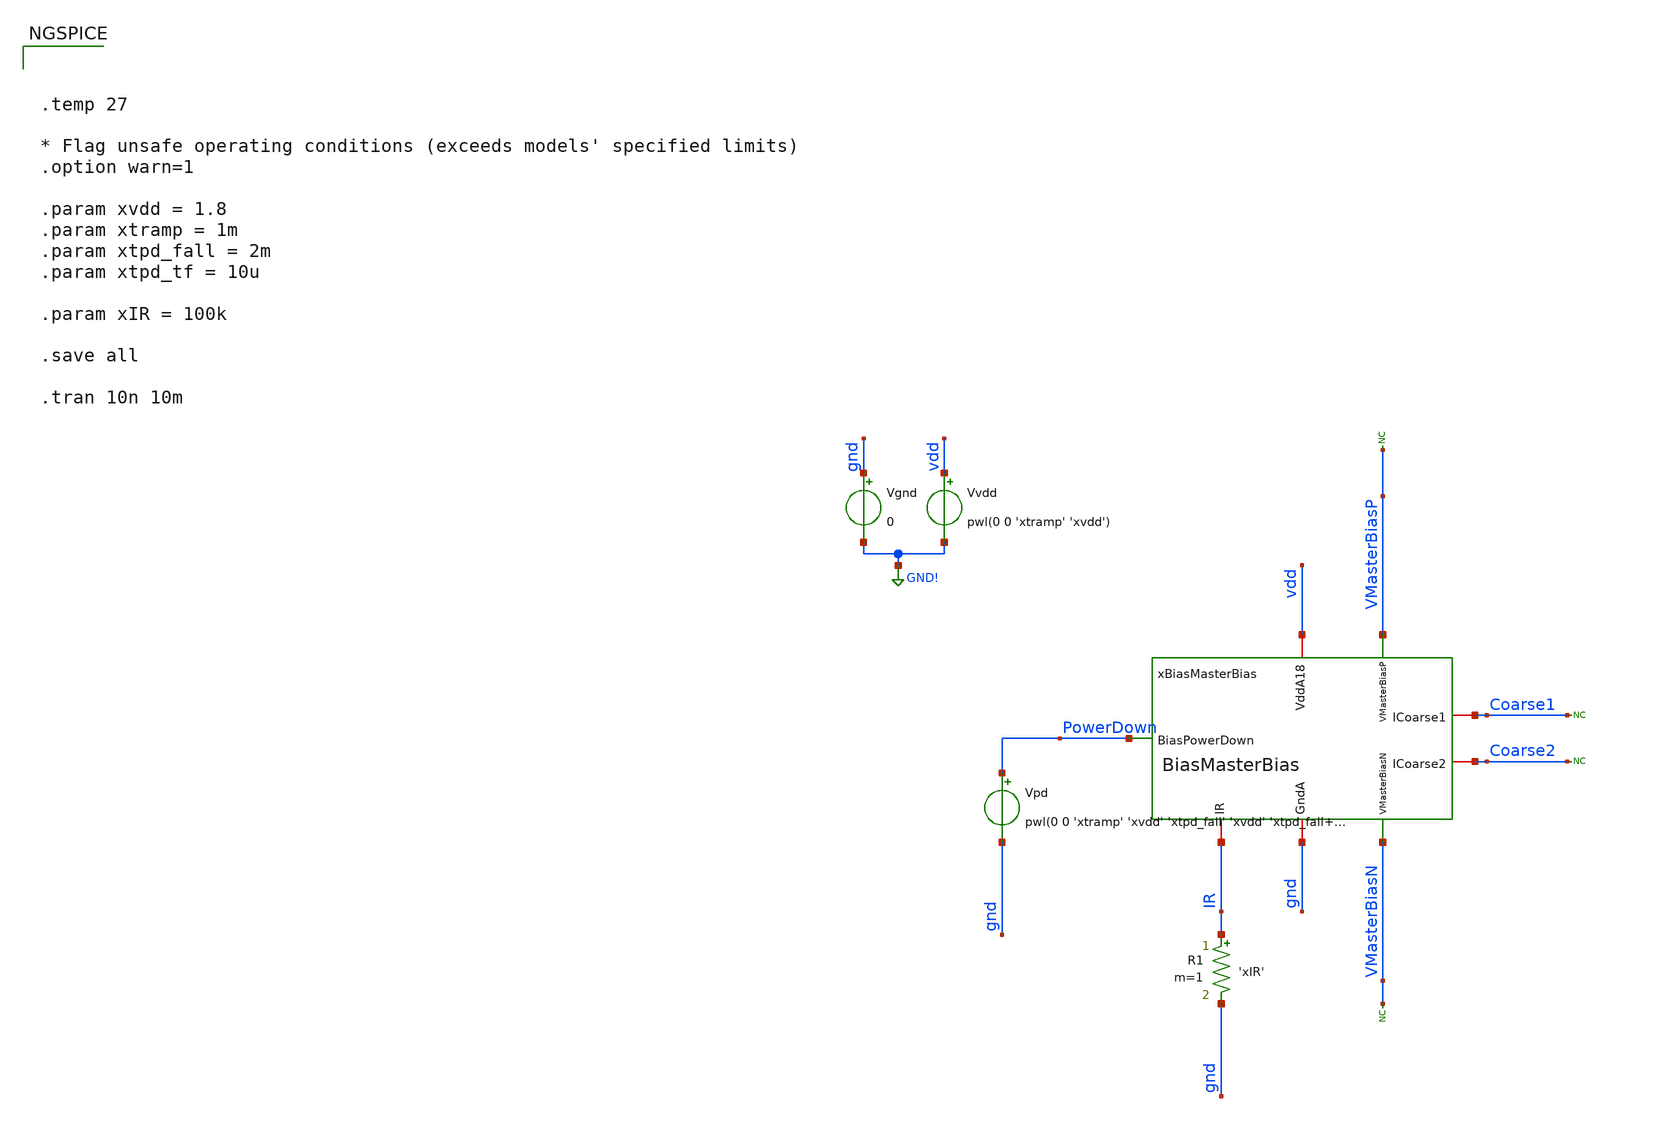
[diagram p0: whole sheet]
** sch_path: analog/klayout/production/final_merge_20260923/testbenches/cace/analog/xschem/tb_BiasMasterBias_bootstrap.sch
**.subckt tb_BiasMasterBias_bootstrap
xBiasMasterBias VMasterBiasP Coarse2 Coarse1 VMasterBiasN PowerDown vdd gnd IR BiasMasterBias
Vgnd gnd GND! 0
.save i(vgnd)
Vvdd vdd GND! pwl(0 0 'xtramp' 'xvdd')
.save i(vvdd)
* noconn VMasterBiasP
* noconn Coarse1
* noconn Coarse2
* noconn VMasterBiasN
R1 IR gnd 'xIR' m=1
Vpd PowerDown gnd pwl(0 0 'xtramp' 'xvdd' 'xtpd_fall' 'xvdd' 'xtpd_fall+xtpd_tf' 0)
.save i(vpd)
**** begin user architecture code

** opencircuitdesign pdks install
.lib $::SKYWATER_MODELS/sky130.lib.spice tt




.temp 27

* Flag unsafe operating conditions (exceeds models' specified limits)
.option warn=1

.param xvdd = 1.8
.param xtramp = 1m
.param xtpd_fall = 2m
.param xtpd_tf = 10u

.param xIR = 100k

.save all

.tran 10n 10m


**** end user architecture code
**.ends

* expanding   symbol:  BiasMasterBias.sym # of pins=8
** sym_path: analog/xschem/BiasMasterBias.sym
** sch_path: analog/xschem/BiasMasterBias.sch
.subckt BiasMasterBias VMasterBiasP ICoarse2 ICoarse1 VMasterBiasN BiasPowerDown VddA18 GndA IR
*.opin VMasterBiasP
*.iopin IR
*.iopin VddA18
*.iopin GndA
*.opin VMasterBiasN
*.iopin ICoarse1
*.iopin ICoarse2
*.ipin BiasPowerDown
XMNBiasDio VMasterBiasN VMasterBiasN GndA GndA sky130_fd_pr__nfet_01v8_lvt L=5 W=20 nf=1 ad='int((1 +
+ 1)/2) * 20 / 1 * 0.29' as='int((1 + 2)/2) * 20 / 1 * 0.29' pd='2*int((1 + 1)/2) * (20 / 1 + 0.29)' ps='2*int((1
+ + 2)/2) * (20 / 1 + 0.29)' nrd='0.29 / 20 ' nrs='0.29 / 20 ' sa=0 sb=0 sd=0 mult=12 m=12
XMPBias VCasc VMasterBiasP VddA18 VddA18 sky130_fd_pr__pfet_01v8 L=20 W=2 nf=1 ad='int((1 + 1)/2) * 2
+ / 1 * 0.29' as='int((1 + 2)/2) * 2 / 1 * 0.29' pd='2*int((1 + 1)/2) * (2 / 1 + 0.29)' ps='2*int((1 +
+ 2)/2) * (2 / 1 + 0.29)' nrd='0.29 / 2 ' nrs='0.29 / 2 ' sa=0 sb=0 sd=0 mult=8 m=8
XMNBias net1 VMasterBiasN IR GndA sky130_fd_pr__nfet_01v8_lvt L=5 W=20 nf=1 ad='int((1 + 1)/2) * 20 /
+ 1 * 0.29' as='int((1 + 2)/2) * 20 / 1 * 0.29' pd='2*int((1 + 1)/2) * (20 / 1 + 0.29)' ps='2*int((1 +
+ 2)/2) * (20 / 1 + 0.29)' nrd='0.29 / 20 ' nrs='0.29 / 20 ' sa=0 sb=0 sd=0 mult=16 m=16
XMnBiasCascDio VCasc VCasc VMasterBiasN GndA sky130_fd_pr__nfet_01v8_lvt L=20 W=1 nf=1 ad='int((1 + 1)/2)
+ * 1 / 1 * 0.29' as='int((1 + 2)/2) * 1 / 1 * 0.29' pd='2*int((1 + 1)/2) * (1 / 1 + 0.29)' ps='2*int((1
+ + 2)/2) * (1 / 1 + 0.29)' nrd='0.29 / 1 ' nrs='0.29 / 1 ' sa=0 sb=0 sd=0 mult=12 m=12
XMnBiasCasc VMasterBiasP VCasc net1 GndA sky130_fd_pr__nfet_01v8_lvt L=20 W=1 nf=1 ad='int((1 + 1)/2)
+ * 1 / 1 * 0.29' as='int((1 + 2)/2) * 1 / 1 * 0.29' pd='2*int((1 + 1)/2) * (1 / 1 + 0.29)' ps='2*int((1
+ + 2)/2) * (1 / 1 + 0.29)' nrd='0.29 / 1 ' nrs='0.29 / 1 ' sa=0 sb=0 sd=0 mult=16 m=16
XMPBiasDio VMasterBiasP VMasterBiasP VddA18 VddA18 sky130_fd_pr__pfet_01v8 L=20 W=2 nf=1 ad='int((1 +
+ 1)/2) * 2 / 1 * 0.29' as='int((1 + 2)/2) * 2 / 1 * 0.29' pd='2*int((1 + 1)/2) * (2 / 1 + 0.29)' ps='2*int((1
+ + 2)/2) * (2 / 1 + 0.29)' nrd='0.29 / 2 ' nrs='0.29 / 2 ' sa=0 sb=0 sd=0 mult=8 m=8
XMNMirr1 net2 VMasterBiasN GndA GndA sky130_fd_pr__nfet_01v8_lvt L=5 W=20 nf=1 ad='int((1 + 1)/2) * 20
+ / 1 * 0.29' as='int((1 + 2)/2) * 20 / 1 * 0.29' pd='2*int((1 + 1)/2) * (20 / 1 + 0.29)' ps='2*int((1
+ + 2)/2) * (20 / 1 + 0.29)' nrd='0.29 / 20 ' nrs='0.29 / 20 ' sa=0 sb=0 sd=0 mult=1 m=1
XMNMirrCasc1 ICoarse1 VCasc net2 GndA sky130_fd_pr__nfet_01v8_lvt L=20 W=1 nf=1 ad='int((1 + 1)/2) *
+ 1 / 1 * 0.29' as='int((1 + 2)/2) * 1 / 1 * 0.29' pd='2*int((1 + 1)/2) * (1 / 1 + 0.29)' ps='2*int((1
+ + 2)/2) * (1 / 1 + 0.29)' nrd='0.29 / 1 ' nrs='0.29 / 1 ' sa=0 sb=0 sd=0 mult=1 m=1
XMNMirr2 net3 VMasterBiasN GndA GndA sky130_fd_pr__nfet_01v8_lvt L=5 W=20 nf=1 ad='int((1 + 1)/2) * 20
+ / 1 * 0.29' as='int((1 + 2)/2) * 20 / 1 * 0.29' pd='2*int((1 + 1)/2) * (20 / 1 + 0.29)' ps='2*int((1
+ + 2)/2) * (20 / 1 + 0.29)' nrd='0.29 / 20 ' nrs='0.29 / 20 ' sa=0 sb=0 sd=0 mult=1 m=1
XMNMirrCasc2 ICoarse2 VCasc net3 GndA sky130_fd_pr__nfet_01v8_lvt L=20 W=1 nf=1 ad='int((1 + 1)/2) *
+ 1 / 1 * 0.29' as='int((1 + 2)/2) * 1 / 1 * 0.29' pd='2*int((1 + 1)/2) * (1 / 1 + 0.29)' ps='2*int((1
+ + 2)/2) * (1 / 1 + 0.29)' nrd='0.29 / 1 ' nrs='0.29 / 1 ' sa=0 sb=0 sd=0 mult=1 m=1
XMNBSPD VCasc BiasPowerDown GndA GndA sky130_fd_pr__nfet_01v8_lvt L=0.2 W=2 nf=1 ad='int((1 + 1)/2) *
+ 2 / 1 * 0.29' as='int((1 + 2)/2) * 2 / 1 * 0.29' pd='2*int((1 + 1)/2) * (2 / 1 + 0.29)' ps='2*int((1
+ + 2)/2) * (2 / 1 + 0.29)' nrd='0.29 / 2 ' nrs='0.29 / 2 ' sa=0 sb=0 sd=0 mult=1 m=1
XMNBSCapBias VddA18 VMasterBiasP VddA18 GndA sky130_fd_pr__nfet_01v8 L=16 W=16 nf=1 ad='int((1 + 1)/2)
+ * 16 / 1 * 0.29' as='int((1 + 2)/2) * 16 / 1 * 0.29' pd='2*int((1 + 1)/2) * (16 / 1 + 0.29)' ps='2*int((1
+ + 2)/2) * (16 / 1 + 0.29)' nrd='0.29 / 16 ' nrs='0.29 / 16 ' sa=0 sb=0 sd=0 mult=1 m=1
XMPBS bootstrap VMasterBiasP VddA18 VddA18 sky130_fd_pr__pfet_01v8 L=0.2 W=2 nf=1 ad='int((1 + 1)/2)
+ * 2 / 1 * 0.29' as='int((1 + 2)/2) * 2 / 1 * 0.29' pd='2*int((1 + 1)/2) * (2 / 1 + 0.29)' ps='2*int((1
+ + 2)/2) * (2 / 1 + 0.29)' nrd='0.29 / 2 ' nrs='0.29 / 2 ' sa=0 sb=0 sd=0 mult=1 m=1
XMNBSCapBS BiasPowerDown bootstrap BiasPowerDown GndA sky130_fd_pr__nfet_01v8 L=16 W=16 nf=1 ad='int((1
+ + 1)/2) * 16 / 1 * 0.29' as='int((1 + 2)/2) * 16 / 1 * 0.29' pd='2*int((1 + 1)/2) * (16 / 1 + 0.29)' ps='2*int((1
+ + 2)/2) * (16 / 1 + 0.29)' nrd='0.29 / 16 ' nrs='0.29 / 16 ' sa=0 sb=0 sd=0 mult=1 m=1
XMPBSPU VCasc bootstrap VddA18 VddA18 sky130_fd_pr__pfet_01v8 L=0.2 W=2 nf=1 ad='int((1 + 1)/2) * 2 /
+ 1 * 0.29' as='int((1 + 2)/2) * 2 / 1 * 0.29' pd='2*int((1 + 1)/2) * (2 / 1 + 0.29)' ps='2*int((1 + 2)/2)
+ * (2 / 1 + 0.29)' nrd='0.29 / 2 ' nrs='0.29 / 2 ' sa=0 sb=0 sd=0 mult=1 m=1
.ends

.GLOBAL GND!
.end
